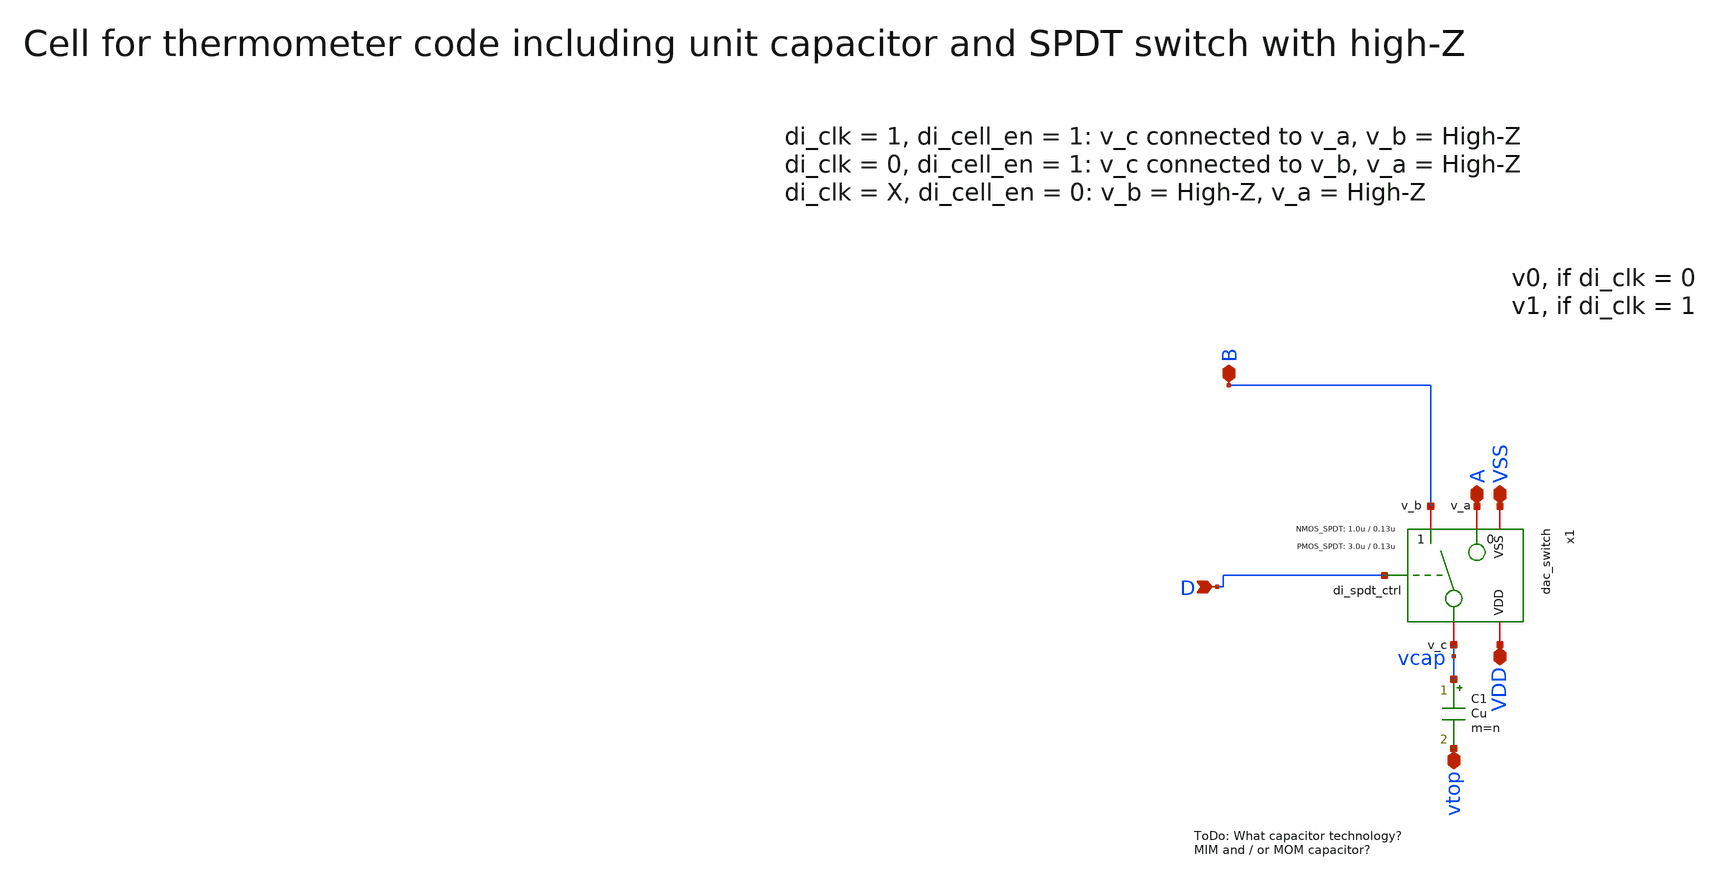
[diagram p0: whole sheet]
** sch_path: xschem/dac_icms_cell/unit_cell.sch
**.subckt unit_cell VSS A VDD D B vtop
*.iopin VSS
*.iopin A
*.iopin VDD
*.ipin D
*.iopin B
*.iopin vtop
x1 VDD D VSS vcap B A dac_switch W_P_TG=3.0u L_P_TG=0.13u W_N_TG=1.0u L_N_TG=0.13u n=n
C1 vcap vtop Cu m=n
**.ends

* expanding   symbol:  dac_icms_cell/dac_switch.sym # of pins=6
** sym_path: xschem/dac_icms_cell/dac_switch.sym
** sch_path: xschem/dac_icms_cell/dac_switch.sch
.subckt dac_switch VDD di_spdt_ctrl VSS v_c v_b v_a  W_P_TG=3.0u L_P_TG=0.13u W_N_TG=1.0u
+ L_N_TG=0.13u n=1
*.iopin v_a
*.iopin v_c
*.iopin VDD
*.iopin VSS
*.ipin di_spdt_ctrl
*.iopin v_b
x1 VDD di_spdt_ctrl_n VSS net2 v_a di_spdt_ctrl transmission_gate_lv_w_dummy W_P=W_P_TG L_P=L_P_TG
+ W_N=W_N_TG L_N=L_N_TG W_P_D=1.0u L_P_D=0.13u W_N_D=1.0u L_N_D=0.13u n=n
x8 VDD di_spdt_ctrl di_spdt_ctrl_n VSS inverter_lv W_P=W_P_TG L_P=L_P_TG W_N=W_N_TG L_N=L_N_TG N_C=1
XM1 net1 v_b VSS VSS sg13_lv_nmos w=0.5u l=0.2u ng=1 m=n mm_ok=1
XM3 net1 v_b VDD VDD sg13_lv_pmos w=1u l=0.2u ng=1 m=n mm_ok=1
x2 VDD di_spdt_ctrl VSS net3 net1 di_spdt_ctrl_n transmission_gate_lv_w_dummy W_P=W_P_TG L_P=L_P_TG
+ W_N=W_N_TG L_N=L_N_TG W_P_D=1.0u L_P_D=0.13u W_N_D=1.0u L_N_D=0.13u n=n
V1 v_c net2 0
V2 v_c net3 0
.ends


* expanding   symbol:  transmission_gate/transmission_gate_lv_w_dummy.sym # of pins=6
** sym_path: xschem/transmission_gate/transmission_gate_lv_w_dummy.sym
** sch_path: xschem/transmission_gate/transmission_gate_lv_w_dummy.sch
.subckt transmission_gate_lv_w_dummy VDD di_tg_ctrl VSS v_b v_a di_tg_ctrl_n  W_P=2.0u L_P=0.13u
+ W_N=2.0u L_N=0.13u W_P_D=1.0u L_P_D=0.13u W_N_D=1.0u L_N_D=0.13u n=1
*.iopin v_a
*.iopin v_b
*.iopin VDD
*.iopin VSS
*.ipin di_tg_ctrl
*.ipin di_tg_ctrl_n
XM1 v_a di_tg_ctrl v_b VSS sg13_lv_nmos w=W_N l=L_N ng=1 m=n mm_ok=1
XM2 v_a di_tg_ctrl_n v_b VDD sg13_lv_pmos w=W_P l=L_P ng=1 m=n mm_ok=1
XMdummy2 v_b di_tg_ctrl v_b VDD sg13_lv_pmos w=W_P l=L_P ng=1 m={n/2} mm_ok=1
XMdummy1 v_b di_tg_ctrl_n v_b VSS sg13_lv_nmos w=W_N l=L_N ng=1 m={n/2} mm_ok=1
.ends


* expanding   symbol:  inverter/inverter_lv.sym # of pins=4
** sym_path: xschem/inverter/inverter_lv.sym
** sch_path: xschem/inverter/inverter_lv.sch
.subckt inverter_lv VDD vin vout VSS  W_P=3.0u L_P=0.13u W_N=1.0u L_N=0.13u N_C=1
*.ipin vin
*.iopin VDD
*.iopin VSS
*.opin vout
XM1 vout vin VDD VDD sg13_lv_pmos w=W_P l=L_P ng=1 m={N_C} mm_ok=1
XM2 vout vin VSS VSS sg13_lv_nmos w=W_N l=L_N ng=1 m={N_C} mm_ok=1
.ends

.end
